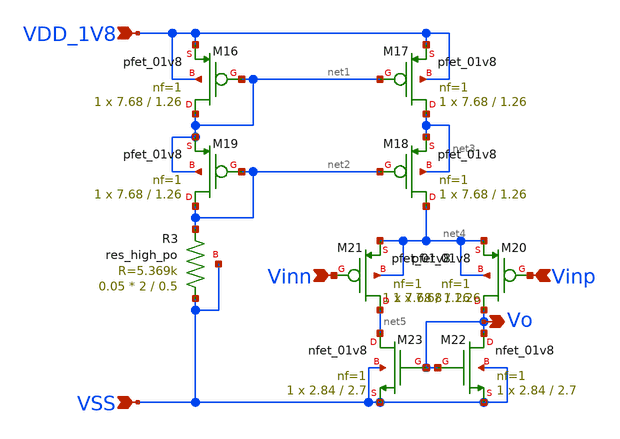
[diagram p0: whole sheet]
** sch_path: design/CNR_GR06_SKY130NM/New_OTA.sch
**.subckt New_OTA VDD_1V8 VSS Vinn Vinp Vo
*.ipin VDD_1V8
*.ipin VSS
*.ipin Vinn
*.ipin Vinp
*.opin Vo
XM16 net1 net1 VDD_1V8 VDD_1V8 sky130_fd_pr__pfet_01v8 L=1.26 W=7.68 nf=1 ad='int((nf+1)/2) * W/nf * 0.29'
+ as='int((nf+2)/2) * W/nf * 0.29' pd='2*int((nf+1)/2) * (W/nf + 0.29)' ps='2*int((nf+2)/2) * (W/nf + 0.29)'
+ nrd='0.29 / W' nrs='0.29 / W' sa=0 sb=0 sd=0 mult=1 m=1
XM17 net3 net1 VDD_1V8 VDD_1V8 sky130_fd_pr__pfet_01v8 L=1.26 W=7.68 nf=1 ad='int((nf+1)/2) * W/nf * 0.29'
+ as='int((nf+2)/2) * W/nf * 0.29' pd='2*int((nf+1)/2) * (W/nf + 0.29)' ps='2*int((nf+2)/2) * (W/nf + 0.29)'
+ nrd='0.29 / W' nrs='0.29 / W' sa=0 sb=0 sd=0 mult=1 m=1
XM18 net4 net2 net3 net3 sky130_fd_pr__pfet_01v8 L=1.26 W=7.68 nf=1 ad='int((nf+1)/2) * W/nf * 0.29'
+ as='int((nf+2)/2) * W/nf * 0.29' pd='2*int((nf+1)/2) * (W/nf + 0.29)' ps='2*int((nf+2)/2) * (W/nf + 0.29)'
+ nrd='0.29 / W' nrs='0.29 / W' sa=0 sb=0 sd=0 mult=1 m=1
XM19 net2 net2 net1 net1 sky130_fd_pr__pfet_01v8 L=1.26 W=7.68 nf=1 ad='int((nf+1)/2) * W/nf * 0.29'
+ as='int((nf+2)/2) * W/nf * 0.29' pd='2*int((nf+1)/2) * (W/nf + 0.29)' ps='2*int((nf+2)/2) * (W/nf + 0.29)'
+ nrd='0.29 / W' nrs='0.29 / W' sa=0 sb=0 sd=0 mult=1 m=1
XM20 Vo Vinp net4 net4 sky130_fd_pr__pfet_01v8 L=1.26 W=7.68 nf=1 ad='int((nf+1)/2) * W/nf * 0.29' as='int((nf+2)/2) * W/nf * 0.29'
+ pd='2*int((nf+1)/2) * (W/nf + 0.29)' ps='2*int((nf+2)/2) * (W/nf + 0.29)' nrd='0.29 / W' nrs='0.29 / W'
+ sa=0 sb=0 sd=0 mult=1 m=1
XM21 net5 Vinn net4 net4 sky130_fd_pr__pfet_01v8 L=1.26 W=7.68 nf=1 ad='int((nf+1)/2) * W/nf * 0.29'
+ as='int((nf+2)/2) * W/nf * 0.29' pd='2*int((nf+1)/2) * (W/nf + 0.29)' ps='2*int((nf+2)/2) * (W/nf + 0.29)'
+ nrd='0.29 / W' nrs='0.29 / W' sa=0 sb=0 sd=0 mult=1 m=1
XM22 Vo Vo VSS VSS sky130_fd_pr__nfet_01v8 L=2.7 W=2.84 nf=1 ad='int((nf+1)/2) * W/nf * 0.29' as='int((nf+2)/2) * W/nf * 0.29'
+ pd='2*int((nf+1)/2) * (W/nf + 0.29)' ps='2*int((nf+2)/2) * (W/nf + 0.29)' nrd='0.29 / W' nrs='0.29 / W'
+ sa=0 sb=0 sd=0 mult=1 m=1
XM23 net5 Vo VSS VSS sky130_fd_pr__nfet_01v8 L=2.7 W=2.84 nf=1 ad='int((nf+1)/2) * W/nf * 0.29' as='int((nf+2)/2) * W/nf * 0.29'
+ pd='2*int((nf+1)/2) * (W/nf + 0.29)' ps='2*int((nf+2)/2) * (W/nf + 0.29)' nrd='0.29 / W' nrs='0.29 / W'
+ sa=0 sb=0 sd=0 mult=1 m=1
XR3 VSS net2 VSS sky130_fd_pr__res_high_po W=2 L=0.5 mult=0.05 m=0.05
**.ends
.end
